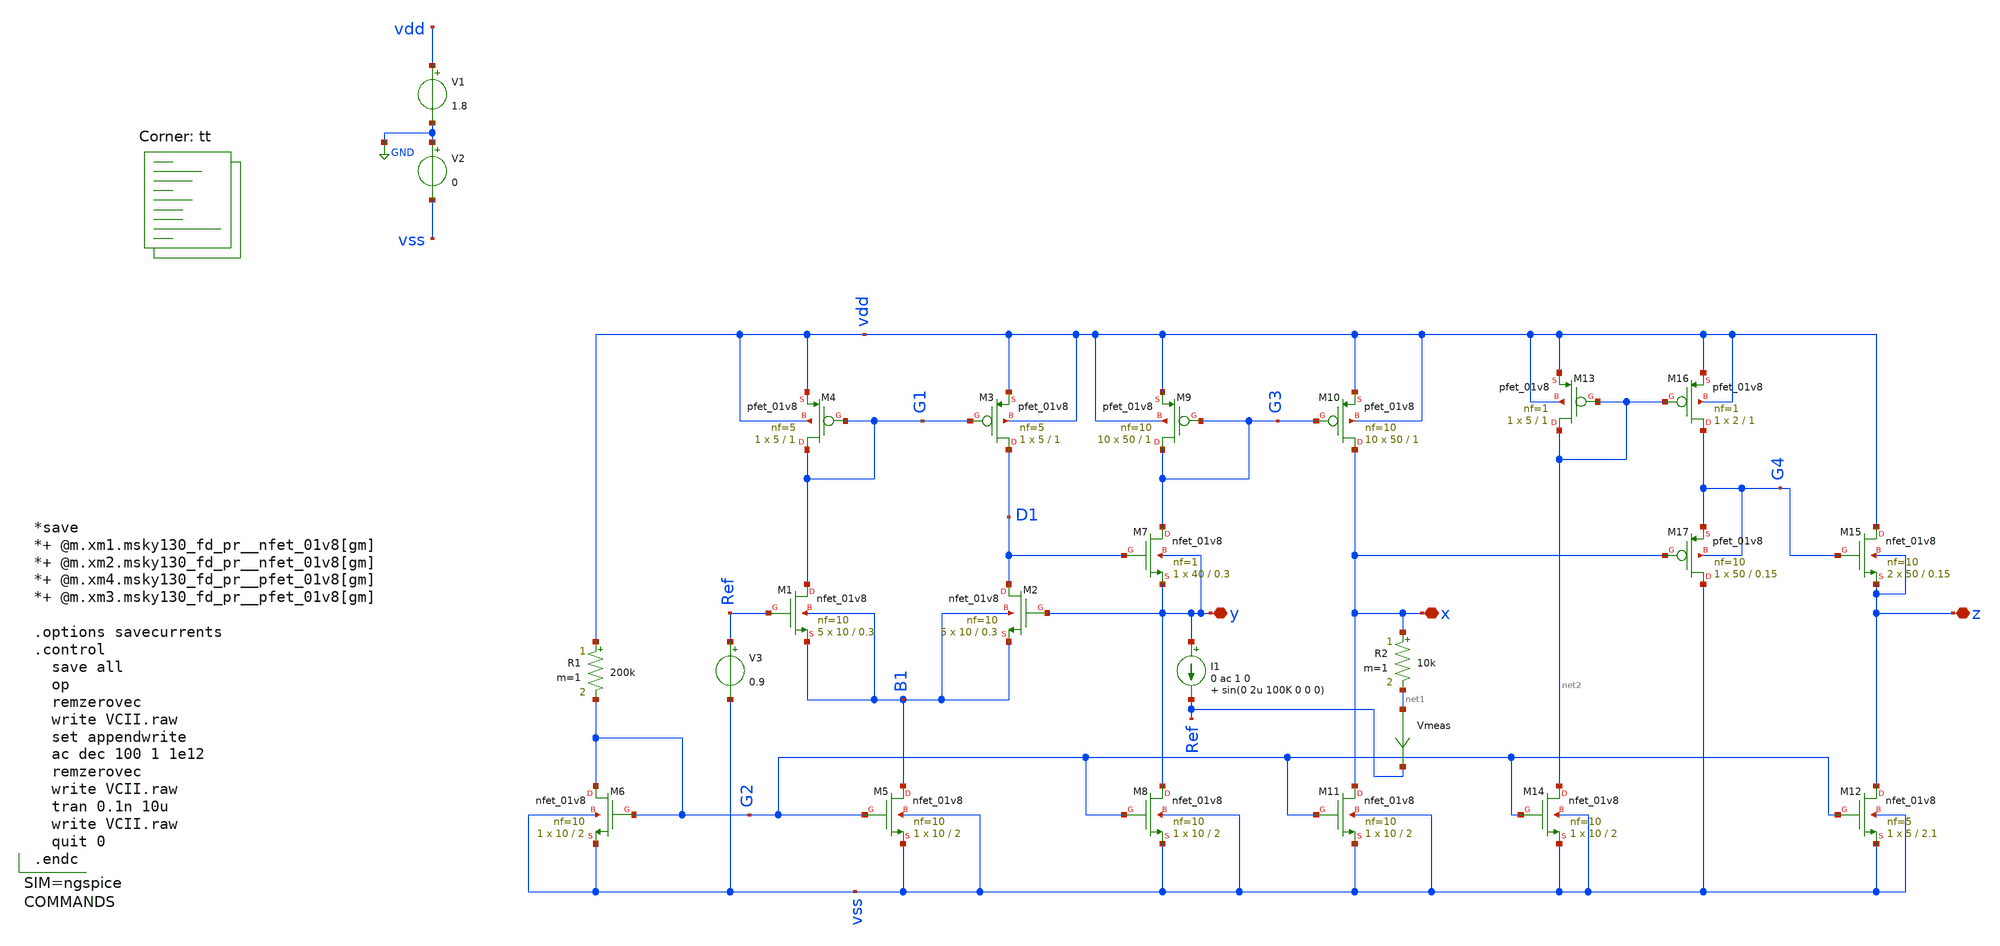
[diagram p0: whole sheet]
** sch_path: xschem/VCII.sch
**.subckt VCII x y z
*.iopin x
*.iopin y
*.iopin z
XM1 G1 Ref B1 B1 sky130_fd_pr__nfet_01v8 L=0.3 W=10 nf=10 ad='int((nf+1)/2) * W/nf * 0.29' as='int((nf+2)/2) * W/nf * 0.29'
+ pd='2*int((nf+1)/2) * (W/nf + 0.29)' ps='2*int((nf+2)/2) * (W/nf + 0.29)' nrd='0.29 / W' nrs='0.29 / W'
+ sa=0 sb=0 sd=0 mult=5 m=5
XM2 D1 y B1 B1 sky130_fd_pr__nfet_01v8 L=0.3 W=10 nf=10 ad='int((nf+1)/2) * W/nf * 0.29' as='int((nf+2)/2) * W/nf * 0.29'
+ pd='2*int((nf+1)/2) * (W/nf + 0.29)' ps='2*int((nf+2)/2) * (W/nf + 0.29)' nrd='0.29 / W' nrs='0.29 / W'
+ sa=0 sb=0 sd=0 mult=5 m=5
XM3 D1 G1 vdd vdd sky130_fd_pr__pfet_01v8 L=1 W=5 nf=5 ad='int((nf+1)/2) * W/nf * 0.29' as='int((nf+2)/2) * W/nf * 0.29'
+ pd='2*int((nf+1)/2) * (W/nf + 0.29)' ps='2*int((nf+2)/2) * (W/nf + 0.29)' nrd='0.29 / W' nrs='0.29 / W'
+ sa=0 sb=0 sd=0 mult=1 m=1
XM4 G1 G1 vdd vdd sky130_fd_pr__pfet_01v8 L=1 W=5 nf=5 ad='int((nf+1)/2) * W/nf * 0.29' as='int((nf+2)/2) * W/nf * 0.29'
+ pd='2*int((nf+1)/2) * (W/nf + 0.29)' ps='2*int((nf+2)/2) * (W/nf + 0.29)' nrd='0.29 / W' nrs='0.29 / W'
+ sa=0 sb=0 sd=0 mult=1 m=1
V1 vdd GND 1.8
V2 GND vss 0
XM5 B1 G2 vss vss sky130_fd_pr__nfet_01v8 L=2 W=10 nf=10 ad='int((nf+1)/2) * W/nf * 0.29' as='int((nf+2)/2) * W/nf * 0.29'
+ pd='2*int((nf+1)/2) * (W/nf + 0.29)' ps='2*int((nf+2)/2) * (W/nf + 0.29)' nrd='0.29 / W' nrs='0.29 / W'
+ sa=0 sb=0 sd=0 mult=1 m=1
XM6 G2 G2 vss vss sky130_fd_pr__nfet_01v8 L=2 W=10 nf=10 ad='int((nf+1)/2) * W/nf * 0.29' as='int((nf+2)/2) * W/nf * 0.29'
+ pd='2*int((nf+1)/2) * (W/nf + 0.29)' ps='2*int((nf+2)/2) * (W/nf + 0.29)' nrd='0.29 / W' nrs='0.29 / W'
+ sa=0 sb=0 sd=0 mult=1 m=1
R1 vdd G2 200k m=1
XM7 G3 D1 y y sky130_fd_pr__nfet_01v8 L=0.3 W=40 nf=1 ad='int((nf+1)/2) * W/nf * 0.29' as='int((nf+2)/2) * W/nf * 0.29'
+ pd='2*int((nf+1)/2) * (W/nf + 0.29)' ps='2*int((nf+2)/2) * (W/nf + 0.29)' nrd='0.29 / W' nrs='0.29 / W'
+ sa=0 sb=0 sd=0 mult=1 m=1
XM8 y G2 vss vss sky130_fd_pr__nfet_01v8 L=2 W=10 nf=10 ad='int((nf+1)/2) * W/nf * 0.29' as='int((nf+2)/2) * W/nf * 0.29'
+ pd='2*int((nf+1)/2) * (W/nf + 0.29)' ps='2*int((nf+2)/2) * (W/nf + 0.29)' nrd='0.29 / W' nrs='0.29 / W'
+ sa=0 sb=0 sd=0 mult=1 m=1
XM9 G3 G3 vdd vdd sky130_fd_pr__pfet_01v8 L=1 W=50 nf=10 ad='int((nf+1)/2) * W/nf * 0.29' as='int((nf+2)/2) * W/nf * 0.29'
+ pd='2*int((nf+1)/2) * (W/nf + 0.29)' ps='2*int((nf+2)/2) * (W/nf + 0.29)' nrd='0.29 / W' nrs='0.29 / W'
+ sa=0 sb=0 sd=0 mult=10 m=10
XM10 x G3 vdd vdd sky130_fd_pr__pfet_01v8 L=1 W=50 nf=10 ad='int((nf+1)/2) * W/nf * 0.29' as='int((nf+2)/2) * W/nf * 0.29'
+ pd='2*int((nf+1)/2) * (W/nf + 0.29)' ps='2*int((nf+2)/2) * (W/nf + 0.29)' nrd='0.29 / W' nrs='0.29 / W'
+ sa=0 sb=0 sd=0 mult=10 m=10
XM11 x G2 vss vss sky130_fd_pr__nfet_01v8 L=2 W=10 nf=10 ad='int((nf+1)/2) * W/nf * 0.29' as='int((nf+2)/2) * W/nf * 0.29'
+ pd='2*int((nf+1)/2) * (W/nf + 0.29)' ps='2*int((nf+2)/2) * (W/nf + 0.29)' nrd='0.29 / W' nrs='0.29 / W'
+ sa=0 sb=0 sd=0 mult=1 m=1
V3 Ref vss 0.9
XM14 net2 G2 vss vss sky130_fd_pr__nfet_01v8 L=2 W=10 nf=10 ad='int((nf+1)/2) * W/nf * 0.29' as='int((nf+2)/2) * W/nf * 0.29'
+ pd='2*int((nf+1)/2) * (W/nf + 0.29)' ps='2*int((nf+2)/2) * (W/nf + 0.29)' nrd='0.29 / W' nrs='0.29 / W'
+ sa=0 sb=0 sd=0 mult=1 m=1
I1 y Ref 0 ac 1 0 sin(0 2u 100K 0 0 0)
R2 x net1 10k m=1
Vmeas net1 Ref 0
.save i(vmeas)
XM12 z G2 vss vss sky130_fd_pr__nfet_01v8 L=2.1 W=5 nf=5 ad='int((nf+1)/2) * W/nf * 0.29' as='int((nf+2)/2) * W/nf * 0.29'
+ pd='2*int((nf+1)/2) * (W/nf + 0.29)' ps='2*int((nf+2)/2) * (W/nf + 0.29)' nrd='0.29 / W' nrs='0.29 / W'
+ sa=0 sb=0 sd=0 mult=1 m=1
XM15 vdd G4 z z sky130_fd_pr__nfet_01v8 L=0.15 W=50 nf=10 ad='int((nf+1)/2) * W/nf * 0.29' as='int((nf+2)/2) * W/nf * 0.29'
+ pd='2*int((nf+1)/2) * (W/nf + 0.29)' ps='2*int((nf+2)/2) * (W/nf + 0.29)' nrd='0.29 / W' nrs='0.29 / W'
+ sa=0 sb=0 sd=0 mult=2 m=2
XM13 net2 net2 vdd vdd sky130_fd_pr__pfet_01v8 L=1 W=5 nf=1 ad='int((nf+1)/2) * W/nf * 0.29' as='int((nf+2)/2) * W/nf * 0.29'
+ pd='2*int((nf+1)/2) * (W/nf + 0.29)' ps='2*int((nf+2)/2) * (W/nf + 0.29)' nrd='0.29 / W' nrs='0.29 / W'
+ sa=0 sb=0 sd=0 mult=1 m=1
XM16 G4 net2 vdd vdd sky130_fd_pr__pfet_01v8 L=1 W=2 nf=1 ad='int((nf+1)/2) * W/nf * 0.29' as='int((nf+2)/2) * W/nf * 0.29'
+ pd='2*int((nf+1)/2) * (W/nf + 0.29)' ps='2*int((nf+2)/2) * (W/nf + 0.29)' nrd='0.29 / W' nrs='0.29 / W'
+ sa=0 sb=0 sd=0 mult=1 m=1
XM17 vss x G4 G4 sky130_fd_pr__pfet_01v8 L=0.15 W=50 nf=10 ad='int((nf+1)/2) * W/nf * 0.29' as='int((nf+2)/2) * W/nf * 0.29'
+ pd='2*int((nf+1)/2) * (W/nf + 0.29)' ps='2*int((nf+2)/2) * (W/nf + 0.29)' nrd='0.29 / W' nrs='0.29 / W'
+ sa=0 sb=0 sd=0 mult=1 m=1
**** begin user architecture code



*save
*+ @m.xm1.msky130_fd_pr__nfet_01v8[gm]
*+ @m.xm2.msky130_fd_pr__nfet_01v8[gm]
*+ @m.xm4.msky130_fd_pr__pfet_01v8[gm]
*+ @m.xm3.msky130_fd_pr__pfet_01v8[gm]

.options savecurrents
.control
  save all
  op
  remzerovec
  write VCII.raw
  set appendwrite
  ac dec 100 1 1e12
  remzerovec
  write VCII.raw
  tran 0.1n 10u
  write VCII.raw
  quit 0
.endc



.lib $::SKYWATER_MODELS/sky130.lib.spice tt
**** end user architecture code
**.ends
.GLOBAL GND
.end
